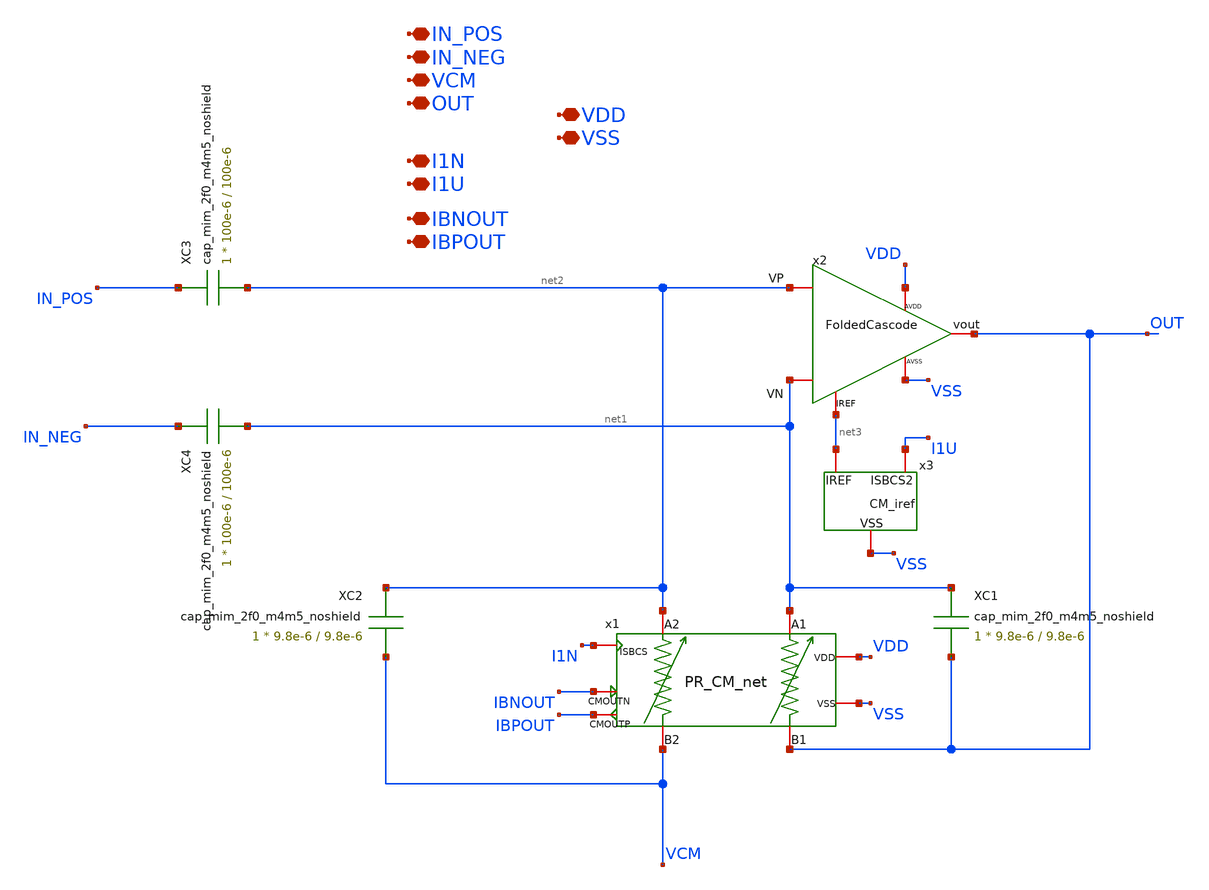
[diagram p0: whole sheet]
** sch_path: TIA_Filter/Filter_TOP.sch
**.subckt Filter_TOP IN_POS IN_NEG I1N I1U VCM OUT IBNOUT IBPOUT VDD VSS
*.iopin IN_POS
*.iopin IN_NEG
*.iopin I1N
*.iopin I1U
*.iopin VCM
*.iopin OUT
*.iopin IBNOUT
*.iopin IBPOUT
*.iopin VDD
*.iopin VSS
XC1 net1 OUT cap_mim_2f0_m4m5_noshield c_width=9.8e-6 c_length=9.8e-6 m=1
XC2 net2 VCM cap_mim_2f0_m4m5_noshield c_width=9.8e-6 c_length=9.8e-6 m=1
XC3 IN_POS net2 cap_mim_2f0_m4m5_noshield c_width=100e-6 c_length=100e-6 m=1
XC4 IN_NEG net1 cap_mim_2f0_m4m5_noshield c_width=100e-6 c_length=100e-6 m=1
x2 net2 net1 OUT net3 VDD VSS FoldedCascode
x3 I1U net3 VSS CM_iref
x1 I1N net1 net2 VCM OUT IBNOUT IBPOUT VDD VSS PR_CM_net
**.ends
.end
